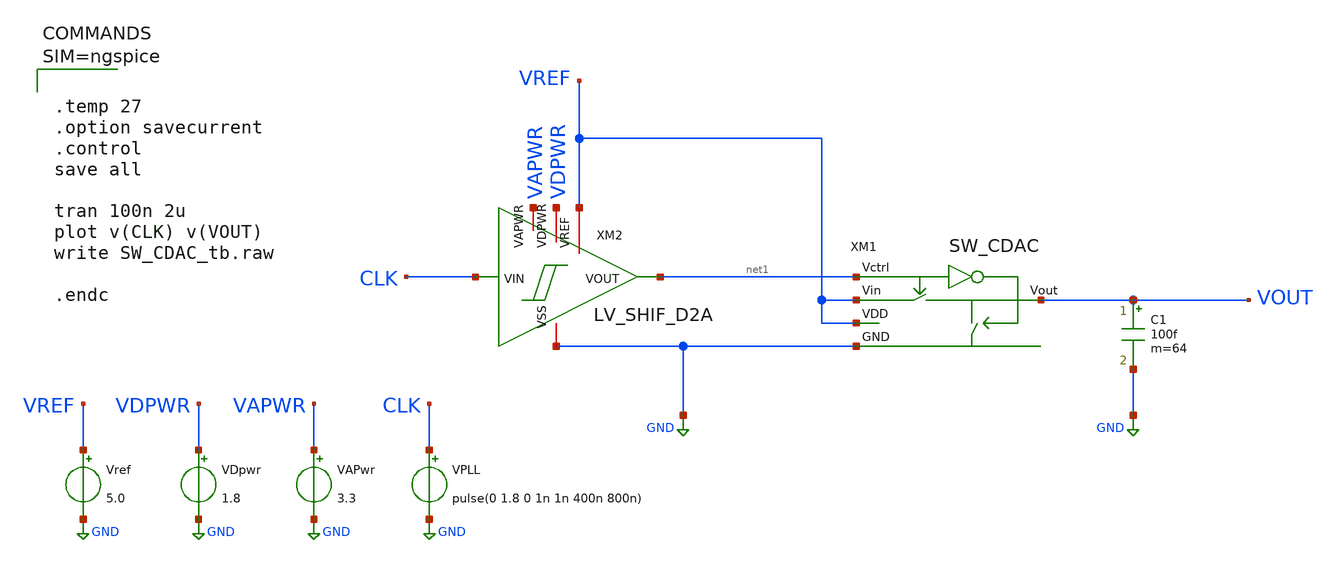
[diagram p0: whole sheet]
** sch_path: xschem/SW_CDAC_tb.sch
**.subckt SW_CDAC_tb
VAPwr VAPWR GND 3.3
Vref VREF GND 5.0
VDpwr VDPWR GND 1.8
XXM1 VREF net1 GND VOUT VREF SW_CDAC
XXM2 VAPWR VDPWR VREF net1 CLK GND LV_SHIF_D2A
VPLL CLK GND pulse(0 1.8 0 1n 1n 400n 800n)
C1 VOUT GND 100f m=64
**** begin user architecture code



.temp 27
.option savecurrent
.control
save all

tran 100n 2u
plot v(CLK) v(VOUT)
write SW_CDAC_tb.raw

.endc




** opencircuitdesign pdks install
.lib $::SKYWATER_MODELS/sky130.lib.spice tt

**** end user architecture code
**.ends

* expanding   symbol:  SW_CDAC.sym # of pins=5
** sym_path: xschem/SW_CDAC.sym
** sch_path: xschem/SW_CDAC.sch
.subckt SW_CDAC VDD Vctrl GND Vout Vin

*.ipin Vctrl
*.ipin Vin
*.opin Vout
*.ipin VDD
*.ipin GND
XM1 Vin net1 Vout VDD sky130_fd_pr__pfet_g5v0d10v5 L=0.5 W=60 nf=1 ad='int((1 + 1)/2) * 60 / 1 * 0.29'
+ as='int((1 + 2)/2) * 60 / 1 * 0.29' pd='2*int((1 + 1)/2) * (60 / 1 + 0.29)' ps='2*int((1 + 2)/2) * (60 / 1 + 0.29)'
+ nrd='0.29 / 60 ' nrs='0.29 / 60 ' sa=0 sb=0 sd=0 mult=1 m=1
XM2 Vin Vctrl Vout GND sky130_fd_pr__nfet_g5v0d10v5 L=0.5 W=30 nf=1 ad='int((1 + 1)/2) * 30 / 1 * 0.29'
+ as='int((1 + 2)/2) * 30 / 1 * 0.29' pd='2*int((1 + 1)/2) * (30 / 1 + 0.29)' ps='2*int((1 + 2)/2) * (30 / 1 + 0.29)'
+ nrd='0.29 / 30 ' nrs='0.29 / 30 ' sa=0 sb=0 sd=0 mult=1 m=1
XM3 net1 Vctrl VDD VDD sky130_fd_pr__pfet_g5v0d10v5 L=0.5 W=60 nf=1 ad='int((1 + 1)/2) * 60 / 1 * 0.29'
+ as='int((1 + 2)/2) * 60 / 1 * 0.29' pd='2*int((1 + 1)/2) * (60 / 1 + 0.29)' ps='2*int((1 + 2)/2) * (60 / 1 + 0.29)'
+ nrd='0.29 / 60 ' nrs='0.29 / 60 ' sa=0 sb=0 sd=0 mult=1 m=1
XM4 net1 Vctrl GND GND sky130_fd_pr__nfet_g5v0d10v5 L=0.5 W=30 nf=1 ad='int((1 + 1)/2) * 30 / 1 * 0.29'
+ as='int((1 + 2)/2) * 30 / 1 * 0.29' pd='2*int((1 + 1)/2) * (30 / 1 + 0.29)' ps='2*int((1 + 2)/2) * (30 / 1 + 0.29)'
+ nrd='0.29 / 30 ' nrs='0.29 / 30 ' sa=0 sb=0 sd=0 mult=1 m=1
XM5 Vout net1 GND GND sky130_fd_pr__nfet_g5v0d10v5 L=0.5 W=30 nf=1 ad='int((1 + 1)/2) * 30 / 1 * 0.29'
+ as='int((1 + 2)/2) * 30 / 1 * 0.29' pd='2*int((1 + 1)/2) * (30 / 1 + 0.29)' ps='2*int((1 + 2)/2) * (30 / 1 + 0.29)'
+ nrd='0.29 / 30 ' nrs='0.29 / 30 ' sa=0 sb=0 sd=0 mult=1 m=1
.ends


* expanding   symbol:  LV_SHIF_D2A.sym # of pins=6
** sym_path: xschem/LV_SHIF_D2A.sym
** sch_path: xschem/LV_SHIF_D2A.sch
.subckt LV_SHIF_D2A VAPWR VDPWR VREF VOUT VIN VSS


*.iopin VDPWR
*.iopin VSS
*.iopin VAPWR
*.iopin VREF
*.ipin VIN
*.opin VOUT
XM2 net1 VIN VSS VSS sky130_fd_pr__nfet_g5v0d10v5 L=0.5 W=2 nf=1 ad='int((1 + 1)/2) * 2 / 1 * 0.29' as='int((1 + 2)/2) * 2 / 1 * 0.29'
+ pd='2*int((1 + 1)/2) * (2 / 1 + 0.29)' ps='2*int((1 + 2)/2) * (2 / 1 + 0.29)' nrd='0.29 / 2 ' nrs='0.29 / 2 '
+ sa=0 sb=0 sd=0 mult=1 m=1
XM1 net1 VIN VDPWR VDPWR sky130_fd_pr__pfet_g5v0d10v5 L=0.5 W=5 nf=1 ad='int((1 + 1)/2) * 5 / 1 * 0.29'
+ as='int((1 + 2)/2) * 5 / 1 * 0.29' pd='2*int((1 + 1)/2) * (5 / 1 + 0.29)' ps='2*int((1 + 2)/2) * (5 / 1 + 0.29)'
+ nrd='0.29 / 5 ' nrs='0.29 / 5 ' sa=0 sb=0 sd=0 mult=1 m=1
XM3 net2 net1 VSS VSS sky130_fd_pr__nfet_g5v0d10v5 L=0.5 W=2 nf=1 ad='int((1 + 1)/2) * 2 / 1 * 0.29'
+ as='int((1 + 2)/2) * 2 / 1 * 0.29' pd='2*int((1 + 1)/2) * (2 / 1 + 0.29)' ps='2*int((1 + 2)/2) * (2 / 1 + 0.29)'
+ nrd='0.29 / 2 ' nrs='0.29 / 2 ' sa=0 sb=0 sd=0 mult=1 m=1
XM4 net2 net1 VDPWR VDPWR sky130_fd_pr__pfet_g5v0d10v5 L=0.5 W=5 nf=1 ad='int((1 + 1)/2) * 5 / 1 * 0.29'
+ as='int((1 + 2)/2) * 5 / 1 * 0.29' pd='2*int((1 + 1)/2) * (5 / 1 + 0.29)' ps='2*int((1 + 2)/2) * (5 / 1 + 0.29)'
+ nrd='0.29 / 5 ' nrs='0.29 / 5 ' sa=0 sb=0 sd=0 mult=1 m=1
XM5 net3 net2 VSS VSS sky130_fd_pr__nfet_g5v0d10v5 L=0.5 W=4 nf=1 ad='int((1 + 1)/2) * 4 / 1 * 0.29'
+ as='int((1 + 2)/2) * 4 / 1 * 0.29' pd='2*int((1 + 1)/2) * (4 / 1 + 0.29)' ps='2*int((1 + 2)/2) * (4 / 1 + 0.29)'
+ nrd='0.29 / 4 ' nrs='0.29 / 4 ' sa=0 sb=0 sd=0 mult=1 m=1
XM6 net3 net2 VAPWR VAPWR sky130_fd_pr__pfet_g5v0d10v5 L=0.5 W=10 nf=1 ad='int((1 + 1)/2) * 10 / 1 * 0.29'
+ as='int((1 + 2)/2) * 10 / 1 * 0.29' pd='2*int((1 + 1)/2) * (10 / 1 + 0.29)' ps='2*int((1 + 2)/2) * (10 / 1 + 0.29)'
+ nrd='0.29 / 10 ' nrs='0.29 / 10 ' sa=0 sb=0 sd=0 mult=1 m=1
XM7 net4 net3 VSS VSS sky130_fd_pr__nfet_g5v0d10v5 L=0.5 W=4 nf=1 ad='int((1 + 1)/2) * 4 / 1 * 0.29'
+ as='int((1 + 2)/2) * 4 / 1 * 0.29' pd='2*int((1 + 1)/2) * (4 / 1 + 0.29)' ps='2*int((1 + 2)/2) * (4 / 1 + 0.29)'
+ nrd='0.29 / 4 ' nrs='0.29 / 4 ' sa=0 sb=0 sd=0 mult=1 m=1
XM8 net4 net3 VAPWR VAPWR sky130_fd_pr__pfet_g5v0d10v5 L=0.5 W=10 nf=1 ad='int((1 + 1)/2) * 10 / 1 * 0.29'
+ as='int((1 + 2)/2) * 10 / 1 * 0.29' pd='2*int((1 + 1)/2) * (10 / 1 + 0.29)' ps='2*int((1 + 2)/2) * (10 / 1 + 0.29)'
+ nrd='0.29 / 10 ' nrs='0.29 / 10 ' sa=0 sb=0 sd=0 mult=1 m=1
XM9 net5 net4 VSS VSS sky130_fd_pr__nfet_g5v0d10v5 L=0.5 W=8 nf=1 ad='int((1 + 1)/2) * 8 / 1 * 0.29'
+ as='int((1 + 2)/2) * 8 / 1 * 0.29' pd='2*int((1 + 1)/2) * (8 / 1 + 0.29)' ps='2*int((1 + 2)/2) * (8 / 1 + 0.29)'
+ nrd='0.29 / 8 ' nrs='0.29 / 8 ' sa=0 sb=0 sd=0 mult=1 m=1
XM10 net5 net4 VREF VREF sky130_fd_pr__pfet_g5v0d10v5 L=0.5 W=20 nf=1 ad='int((1 + 1)/2) * 20 / 1 * 0.29'
+ as='int((1 + 2)/2) * 20 / 1 * 0.29' pd='2*int((1 + 1)/2) * (20 / 1 + 0.29)' ps='2*int((1 + 2)/2) * (20 / 1 + 0.29)'
+ nrd='0.29 / 20 ' nrs='0.29 / 20 ' sa=0 sb=0 sd=0 mult=1 m=1
XM11 VOUT net5 VSS VSS sky130_fd_pr__nfet_g5v0d10v5 L=0.5 W=8 nf=1 ad='int((1 + 1)/2) * 8 / 1 * 0.29'
+ as='int((1 + 2)/2) * 8 / 1 * 0.29' pd='2*int((1 + 1)/2) * (8 / 1 + 0.29)' ps='2*int((1 + 2)/2) * (8 / 1 + 0.29)'
+ nrd='0.29 / 8 ' nrs='0.29 / 8 ' sa=0 sb=0 sd=0 mult=1 m=1
XM12 VOUT net5 VREF VREF sky130_fd_pr__pfet_g5v0d10v5 L=0.5 W=20 nf=1 ad='int((1 + 1)/2) * 20 / 1 * 0.29'
+ as='int((1 + 2)/2) * 20 / 1 * 0.29' pd='2*int((1 + 1)/2) * (20 / 1 + 0.29)' ps='2*int((1 + 2)/2) * (20 / 1 + 0.29)'
+ nrd='0.29 / 20 ' nrs='0.29 / 20 ' sa=0 sb=0 sd=0 mult=1 m=1
.ends

.GLOBAL GND
.end
